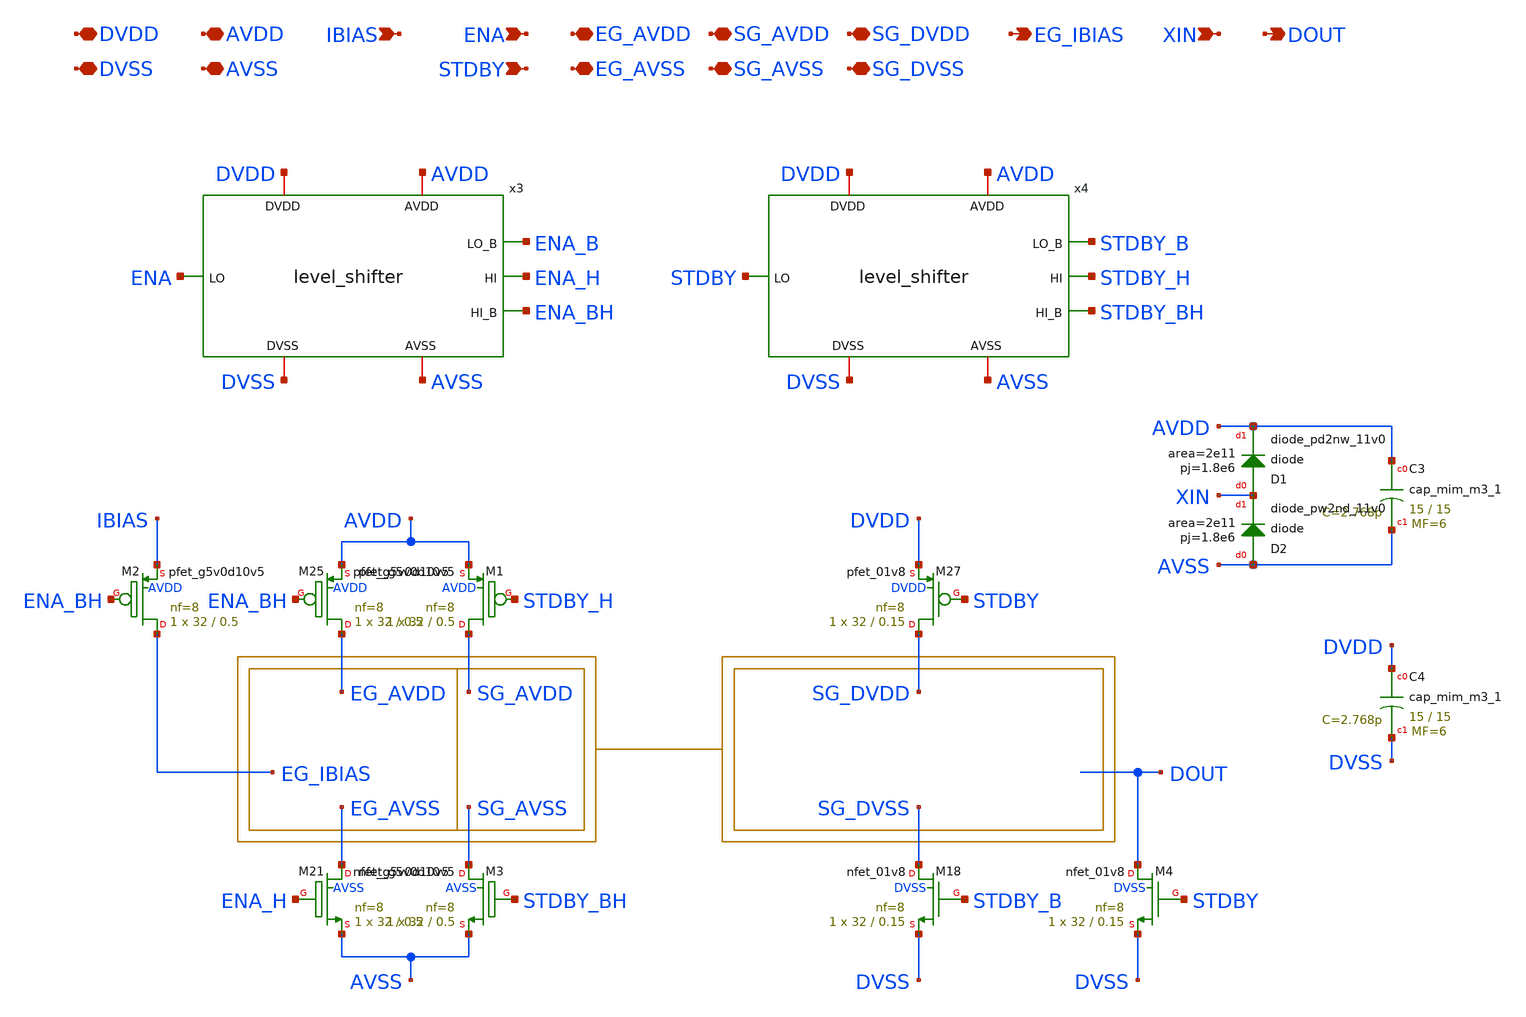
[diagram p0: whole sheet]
** sch_path: xschem/power_gating.sch
**.subckt power_gating DVDD DVSS AVDD AVSS ENA STDBY DOUT IBIAS EG_AVDD EG_AVSS SG_AVDD SG_AVSS
*+ SG_DVDD SG_DVSS EG_IBIAS XIN
*.iopin DVDD
*.iopin DVSS
*.iopin AVDD
*.iopin AVSS
*.ipin ENA
*.ipin STDBY
*.opin DOUT
*.ipin IBIAS
*.iopin EG_AVDD
*.iopin EG_AVSS
*.iopin SG_AVDD
*.iopin SG_AVSS
*.iopin SG_DVDD
*.iopin SG_DVSS
*.opin EG_IBIAS
*.ipin XIN
x3 AVDD ENA_B DVDD ENA ENA_H AVSS DVSS ENA_BH level_shifter
x4 AVDD STDBY_B DVDD STDBY STDBY_H AVSS DVSS STDBY_BH level_shifter
XM18 SG_DVSS STDBY_B DVSS DVSS sky130_fd_pr__nfet_01v8 L=0.15 W=32 nf=8 ad='int((nf+1)/2) * W/nf * 0.29'
+ as='int((nf+2)/2) * W/nf * 0.29' pd='2*int((nf+1)/2) * (W/nf + 0.29)' ps='2*int((nf+2)/2) * (W/nf + 0.29)'
+ nrd='0.29 / W' nrs='0.29 / W' sa=0 sb=0 sd=0 mult=1 m=1
XM21 EG_AVSS ENA_H AVSS AVSS sky130_fd_pr__nfet_g5v0d10v5 L=0.5 W=32 nf=8 ad='int((nf+1)/2) * W/nf * 0.29'
+ as='int((nf+2)/2) * W/nf * 0.29' pd='2*int((nf+1)/2) * (W/nf + 0.29)' ps='2*int((nf+2)/2) * (W/nf + 0.29)'
+ nrd='0.29 / W' nrs='0.29 / W' sa=0 sb=0 sd=0 mult=1 m=1
XM25 EG_AVDD ENA_BH AVDD AVDD sky130_fd_pr__pfet_g5v0d10v5 L=0.5 W=32 nf=8 ad='int((nf+1)/2) * W/nf * 0.29'
+ as='int((nf+2)/2) * W/nf * 0.29' pd='2*int((nf+1)/2) * (W/nf + 0.29)' ps='2*int((nf+2)/2) * (W/nf + 0.29)'
+ nrd='0.29 / W' nrs='0.29 / W' sa=0 sb=0 sd=0 mult=1 m=1
XM27 SG_DVDD STDBY DVDD DVDD sky130_fd_pr__pfet_01v8 L=0.15 W=32 nf=8 ad='int((8 + 1)/2) * 32 / 8 * 0.29'
+ as='int((8 + 2)/2) * 32 / 8 * 0.29' pd='2*int((8 + 1)/2) * (32 / 8 + 0.29)' ps='2*int((8 + 2)/2) * (32 / 8 + 0.29)'
+ nrd='0.29 / 32 ' nrs='0.29 / 32 ' sa=0 sb=0 sd=0 mult=1 m=1
XM1 SG_AVDD STDBY_H AVDD AVDD sky130_fd_pr__pfet_g5v0d10v5 L=0.5 W=32 nf=8 ad='int((nf+1)/2) * W/nf * 0.29'
+ as='int((nf+2)/2) * W/nf * 0.29' pd='2*int((nf+1)/2) * (W/nf + 0.29)' ps='2*int((nf+2)/2) * (W/nf + 0.29)'
+ nrd='0.29 / W' nrs='0.29 / W' sa=0 sb=0 sd=0 mult=1 m=1
XM2 EG_IBIAS ENA_BH IBIAS AVDD sky130_fd_pr__pfet_g5v0d10v5 L=0.5 W=32 nf=8 ad='int((nf+1)/2) * W/nf * 0.29'
+ as='int((nf+2)/2) * W/nf * 0.29' pd='2*int((nf+1)/2) * (W/nf + 0.29)' ps='2*int((nf+2)/2) * (W/nf + 0.29)'
+ nrd='0.29 / W' nrs='0.29 / W' sa=0 sb=0 sd=0 mult=1 m=1
XM3 SG_AVSS STDBY_BH AVSS AVSS sky130_fd_pr__nfet_g5v0d10v5 L=0.5 W=32 nf=8 ad='int((nf+1)/2) * W/nf * 0.29'
+ as='int((nf+2)/2) * W/nf * 0.29' pd='2*int((nf+1)/2) * (W/nf + 0.29)' ps='2*int((nf+2)/2) * (W/nf + 0.29)'
+ nrd='0.29 / W' nrs='0.29 / W' sa=0 sb=0 sd=0 mult=1 m=1
XM4 DOUT STDBY DVSS DVSS sky130_fd_pr__nfet_01v8 L=0.15 W=32 nf=8 ad='int((nf+1)/2) * W/nf * 0.29' as='int((nf+2)/2) * W/nf * 0.29'
+ pd='2*int((nf+1)/2) * (W/nf + 0.29)' ps='2*int((nf+2)/2) * (W/nf + 0.29)' nrd='0.29 / W' nrs='0.29 / W'
+ sa=0 sb=0 sd=0 mult=1 m=1
XC3 AVDD AVSS sky130_fd_pr__cap_mim_m3_1 W=15 L=15 MF=6 m=6
XC4 DVDD DVSS sky130_fd_pr__cap_mim_m3_1 W=15 L=15 MF=6 m=6
XD1 XIN AVDD sky130_fd_pr__diode_pd2nw_11v0 area=2e11 pj=1.8e6
XD2 AVSS XIN sky130_fd_pr__diode_pw2nd_11v0 area=2e11 pj=1.8e6
**.ends

* expanding   symbol:  level_shifter.sym # of pins=8
** sym_path: xschem/level_shifter.sym
** sch_path: xschem/level_shifter.sch
.subckt level_shifter AVDD LO_B DVDD LO HI AVSS DVSS HI_B
*.iopin DVDD
*.iopin DVSS
*.iopin AVDD
*.iopin AVSS
*.ipin LO
*.opin LO_B
*.opin HI
*.opin HI_B
XM18 LO_B LO DVSS DVSS sky130_fd_pr__nfet_01v8 L=0.15 W=1 nf=1 ad='int((nf+1)/2) * W/nf * 0.29' as='int((nf+2)/2) * W/nf * 0.29'
+ pd='2*int((nf+1)/2) * (W/nf + 0.29)' ps='2*int((nf+2)/2) * (W/nf + 0.29)' nrd='0.29 / W' nrs='0.29 / W'
+ sa=0 sb=0 sd=0 mult=1 m=1
XM21 HI_B LO AVSS AVSS sky130_fd_pr__nfet_g5v0d10v5 L=0.5 W=1 nf=1 ad='int((nf+1)/2) * W/nf * 0.29' as='int((nf+2)/2) * W/nf * 0.29'
+ pd='2*int((nf+1)/2) * (W/nf + 0.29)' ps='2*int((nf+2)/2) * (W/nf + 0.29)' nrd='0.29 / W' nrs='0.29 / W'
+ sa=0 sb=0 sd=0 mult=1 m=1
XM25 HI_B HI AVDD AVDD sky130_fd_pr__pfet_g5v0d10v5 L=0.5 W=1 nf=1 ad='int((nf+1)/2) * W/nf * 0.29' as='int((nf+2)/2) * W/nf * 0.29'
+ pd='2*int((nf+1)/2) * (W/nf + 0.29)' ps='2*int((nf+2)/2) * (W/nf + 0.29)' nrd='0.29 / W' nrs='0.29 / W'
+ sa=0 sb=0 sd=0 mult=1 m=1
XM27 LO_B LO DVDD DVDD sky130_fd_pr__pfet_01v8 L=0.15 W=1 nf=1 ad='int((1 + 1)/2) * 1 / 1 * 0.29' as='int((1 + 2)/2) * 1 / 1 * 0.29'
+ pd='2*int((1 + 1)/2) * (1 / 1 + 0.29)' ps='2*int((1 + 2)/2) * (1 / 1 + 0.29)' nrd='0.29 / 1 ' nrs='0.29 / 1 '
+ sa=0 sb=0 sd=0 mult=1 m=1
XM1 HI HI_B AVDD AVDD sky130_fd_pr__pfet_g5v0d10v5 L=0.5 W=1 nf=1 ad='int((nf+1)/2) * W/nf * 0.29' as='int((nf+2)/2) * W/nf * 0.29'
+ pd='2*int((nf+1)/2) * (W/nf + 0.29)' ps='2*int((nf+2)/2) * (W/nf + 0.29)' nrd='0.29 / W' nrs='0.29 / W'
+ sa=0 sb=0 sd=0 mult=1 m=1
XM2 HI LO_B AVSS AVSS sky130_fd_pr__nfet_g5v0d10v5 L=0.5 W=1 nf=1 ad='int((nf+1)/2) * W/nf * 0.29' as='int((nf+2)/2) * W/nf * 0.29'
+ pd='2*int((nf+1)/2) * (W/nf + 0.29)' ps='2*int((nf+2)/2) * (W/nf + 0.29)' nrd='0.29 / W' nrs='0.29 / W'
+ sa=0 sb=0 sd=0 mult=1 m=1
.ends

.end
